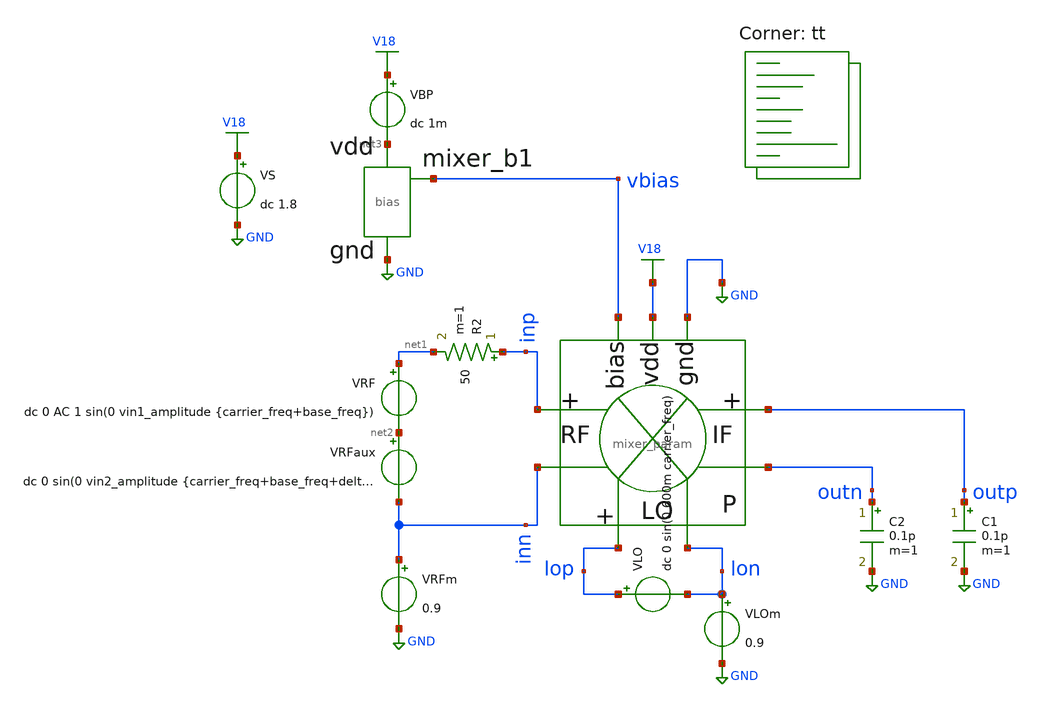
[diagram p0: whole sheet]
** sch_path: xschem/mixer_transfer_tb.sch
**.subckt mixer_transfer_tb
VRF net1 net2 dc 0 AC 1 sin(0 vin1_amplitude {carrier_freq+base_freq})
VLO lop lon dc 0 sin(0 600m carrier_freq)
R2 inp net1 50 m=1
VLOm lon GND 0.9
VRFm inn GND 0.9
VS V18 GND dc 1.8
VBP V18 net3 dc 1m
X1 vbias net3 GND bias
C1 outp GND 0.1p m=1
C2 outn GND 0.1p m=1
VRFaux net2 inn dc 0 sin(0 vin2_amplitude {carrier_freq+base_freq+delta_freq})
X2 inp inn outp outn lon lop vbias V18 GND mixer_param
**** begin user architecture code
.lib $::SKYWATER_MODELS/sky130.lib.spice tt


*.control
*tran 10p 5us
*save all
*write tb_gain.raw
*.endc




.option TRTOL=5
.option SCALE=1e-6

.param carrier_freq=900Meg
.param base_freq=5Meg
.param delta_freq=1Meg
.param vin1_amplitude=10e-3
.param vin2_amplitude=10e-3

.param bias_width=6
.param mixer_biasfactor=10
.param mixer_m23width=52.05
.param mixer_m23fingers=9
.param mixer_m4567width=25.95
.param mixer_m4567fingers=5
.param mixer_rw=5.73
.param mixer_rl=45.9


**** end user architecture code
**.ends

* expanding   symbol:  efabless-opencore/xschem/bias.sym # of pins=3
** sym_path: xschem/bias.sym
** sch_path: xschem/bias.sch
.subckt bias mixer_b1 vdd gnd
*.iopin vdd
*.iopin gnd
*.opin mixer_b1
XM1 net1 mixer_b1 gnd GND sky130_fd_pr__nfet_01v8 L=0.15 W=bias_width nf=1 ad='int((nf+1)/2) * W/nf * 0.29'
+ as='int((nf+2)/2) * W/nf * 0.29' pd='2*int((nf+1)/2) * (W/nf + 0.29)' ps='2*int((nf+2)/2) * (W/nf + 0.29)'
+ nrd='0.29 / W' nrs='0.29 / W' sa=0 sb=0 sd=0 mult=1 m=1
XR1 mixer_b1 vdd gnd sky130_fd_pr__res_xhigh_po_0p35 L=3.5 mult=1 m=1
Vsense mixer_b1 net1 0
.ends


* expanding   symbol:  opensubghz/xschem/mixer_param.sym # of pins=9
** sym_path: xschem/mixer_param.sym
** sch_path: xschem/mixer_param.sch
.subckt mixer_param RFp RFn IFp IFn LOn LOp bias vdd gnd
*.ipin LOp
*.ipin RFp
*.ipin RFn
*.ipin LOn
*.ipin bias
*.iopin gnd
*.iopin vdd
*.opin IFp
*.opin IFn
XM2 net1 RFp cm1 GND sky130_fd_pr__nfet_01v8 L=0.15 W='mixer_m23width' nf='mixer_m23fingers' ad='int((nf+1)/2) * W/nf * 0.29'
+ as='int((nf+2)/2) * W/nf * 0.29' pd='2*int((nf+1)/2) * (W/nf + 0.29)' ps='2*int((nf+2)/2) * (W/nf + 0.29)'
+ nrd='0.29 / W' nrs='0.29 / W' sa=0 sb=0 sd=0 mult=1 m=1
XM1 net2 bias gnd GND sky130_fd_pr__nfet_01v8 L=0.15 W='bias_width*mixer_biasfactor' nf='mixer_biasfactor'
+ ad='int((nf+1)/2) * W/nf * 0.29' as='int((nf+2)/2) * W/nf * 0.29' pd='2*int((nf+1)/2) * (W/nf + 0.29)'
+ ps='2*int((nf+2)/2) * (W/nf + 0.29)' nrd='0.29 / W' nrs='0.29 / W' sa=0 sb=0 sd=0 mult=1 m=1
XM3 net3 RFn cm1 GND sky130_fd_pr__nfet_01v8 L=0.15 W='mixer_m23width' nf='mixer_m23fingers' ad='int((nf+1)/2) * W/nf * 0.29'
+ as='int((nf+2)/2) * W/nf * 0.29' pd='2*int((nf+1)/2) * (W/nf + 0.29)' ps='2*int((nf+2)/2) * (W/nf + 0.29)'
+ nrd='0.29 / W' nrs='0.29 / W' sa=0 sb=0 sd=0 mult=1 m=1
XM4 IFp LOp cm2a GND sky130_fd_pr__nfet_01v8 L=0.15 W='mixer_m4567width' nf='mixer_m4567fingers' ad='int((nf+1)/2) * W/nf * 0.29'
+ as='int((nf+2)/2) * W/nf * 0.29' pd='2*int((nf+1)/2) * (W/nf + 0.29)' ps='2*int((nf+2)/2) * (W/nf + 0.29)'
+ nrd='0.29 / W' nrs='0.29 / W' sa=0 sb=0 sd=0 mult=1 m=1
XM5 IFn LOn cm2a GND sky130_fd_pr__nfet_01v8 L=0.15 W='mixer_m4567width' nf='mixer_m4567fingers' ad='int((nf+1)/2) * W/nf * 0.29'
+ as='int((nf+2)/2) * W/nf * 0.29' pd='2*int((nf+1)/2) * (W/nf + 0.29)' ps='2*int((nf+2)/2) * (W/nf + 0.29)'
+ nrd='0.29 / W' nrs='0.29 / W' sa=0 sb=0 sd=0 mult=1 m=1
XM6 IFp LOn cm2b GND sky130_fd_pr__nfet_01v8 L=0.15 W='mixer_m4567width' nf='mixer_m4567fingers' ad='int((nf+1)/2) * W/nf * 0.29'
+ as='int((nf+2)/2) * W/nf * 0.29' pd='2*int((nf+1)/2) * (W/nf + 0.29)' ps='2*int((nf+2)/2) * (W/nf + 0.29)'
+ nrd='0.29 / W' nrs='0.29 / W' sa=0 sb=0 sd=0 mult=1 m=1
XM7 IFn LOp cm2b GND sky130_fd_pr__nfet_01v8 L=0.15 W='mixer_m4567width' nf='mixer_m4567fingers' ad='int((nf+1)/2) * W/nf * 0.29'
+ as='int((nf+2)/2) * W/nf * 0.29' pd='2*int((nf+1)/2) * (W/nf + 0.29)' ps='2*int((nf+2)/2) * (W/nf + 0.29)'
+ nrd='0.29 / W' nrs='0.29 / W' sa=0 sb=0 sd=0 mult=1 m=1
Vscm1 cm1 net2 dc 0
Vscm2b cm2b net3 dc 0
Vscm2a cm2a net1 dc 0
XR1 IFp vdd gnd sky130_fd_pr__res_xhigh_po_5p73 L='mixer_rl' mult=1 m=1
XR2 IFn vdd gnd sky130_fd_pr__res_xhigh_po_5p73 L='mixer_rl' mult=1 m=1
.ends

.GLOBAL V18
.GLOBAL GND
.end
